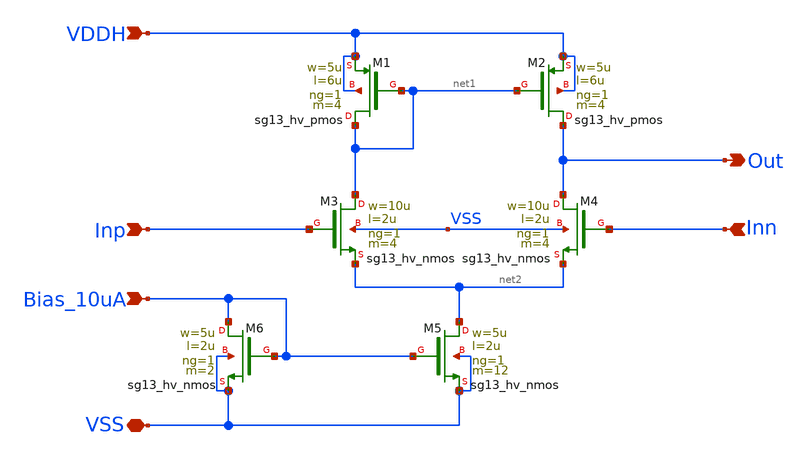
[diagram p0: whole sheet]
** sch_path: sar_adc/xschem/blocks/5t_ota/5T_OTA.sch
**.subckt 5T_OTA VDDH Out VSS Bias_10uA Inp Inn
*.ipin VDDH
*.opin Out
*.iopin VSS
*.ipin Bias_10uA
*.ipin Inp
*.ipin Inn
XM1 net1 net1 VDDH VDDH sg13_hv_pmos w=5u l=6u ng=1 m=4 mm_ok=1
XM2 Out net1 VDDH VDDH sg13_hv_pmos w=5u l=6u ng=1 m=4 mm_ok=1
XM3 net1 Inp net2 VSS sg13_hv_nmos w=10u l=2u ng=1 m=4 mm_ok=1
XM4 Out Inn net2 VSS sg13_hv_nmos w=10u l=2u ng=1 m=4 mm_ok=1
XM5 net2 Bias_10uA VSS VSS sg13_hv_nmos w=5u l=2u ng=1 m=12 mm_ok=1
XM6 Bias_10uA Bias_10uA VSS VSS sg13_hv_nmos w=5u l=2u ng=1 m=2 mm_ok=1
**.ends
.end
